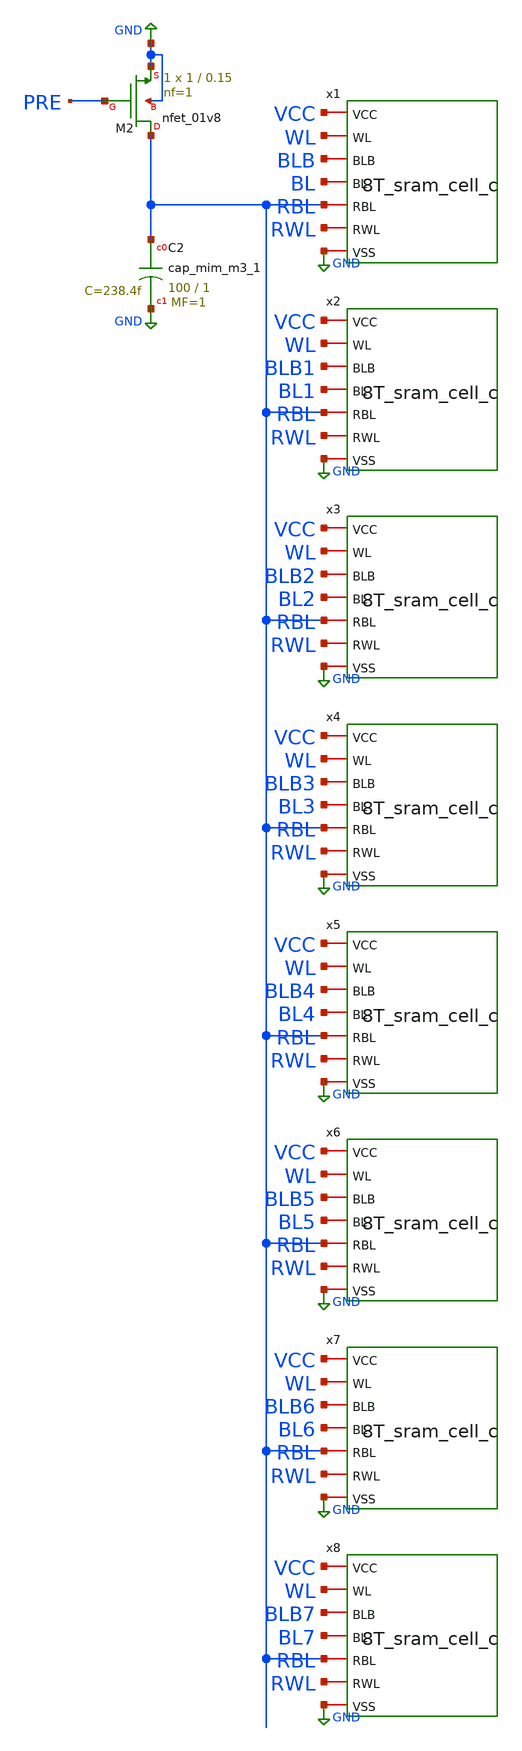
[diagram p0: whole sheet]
** sch_path: 8T_sram_c_array_mactest.sch
**.subckt 8T_sram_c_array_mactest
x1 VCC WL BLB BL RBL RWL GND 8T_sram_cell_c
XC2 RBL GND sky130_fd_pr__cap_mim_m3_1 W=100 L=1 MF=1 m=1
x2 VCC WL BLB1 BL1 RBL RWL GND 8T_sram_cell_c
x3 VCC WL BLB2 BL2 RBL RWL GND 8T_sram_cell_c
x4 VCC WL BLB3 BL3 RBL RWL GND 8T_sram_cell_c
x5 VCC WL BLB4 BL4 RBL RWL GND 8T_sram_cell_c
x6 VCC WL BLB5 BL5 RBL RWL GND 8T_sram_cell_c
x7 VCC WL BLB6 BL6 RBL RWL GND 8T_sram_cell_c
x8 VCC WL BLB7 BL7 RBL RWL GND 8T_sram_cell_c
XM2 RBL PRE GND GND sky130_fd_pr__nfet_01v8 L=0.15 W=1 nf=1 ad='int((1 + 1)/2) * 1 / 1 * 0.29' as='int((1 + 2)/2) * 1 / 1 * 0.29'
+ pd='2*int((1 + 1)/2) * (1 / 1 + 0.29)' ps='2*int((1 + 2)/2) * (1 / 1 + 0.29)' nrd='0.29 / 1 ' nrs='0.29 / 1 '
+ sa=0 sb=0 sd=0 mult=1 m=1
**** begin user architecture code


.param dly=0ns t_dly=2ns raise=10ps fall=10ps BL_period=20ns prds=128 pre_time=2ns read_time=0.5ns

**vss vss 0 DC 0
* PULSE(VSS 1.8 2ns 100ps 100ps 3ns 5ns 4)PULSE(0 1.7 {dly + t_dly/2} {raise} {fall} {(BL_period/2)- t_dly}
*+ {BL_period/2} {prds*2})

V_WL WL 0 PULSE({VSS} {VCC} {dly + t_dly/2} {raise} {fall} {(BL_period/2)- t_dly} {BL_period} {prds*2})


V_BL BLB 0 PULSE({VSS} {VCC} {dly} {raise} {fall} {BL_period} {BL_period*2} {prds})
V_BLB BL 0 PULSE({VCC} {VSS} {dly} {raise} {fall} {BL_period} {BL_period*2} {prds})

V_BL1 BLB1 0 PULSE({VSS} {VCC} {dly} {raise} {fall} {BL_period*2} {BL_period*4} {prds})
V_BLB1 BL1 0 PULSE({VCC} {VSS} {dly} {raise} {fall} {BL_period*2} {BL_period*4} {prds})

V_BL2 BLB2 0 PULSE({VSS} {VCC} {dly} {raise} {fall} {BL_period*4} {BL_period*8} {prds})
V_BLB2 BL2 0 PULSE({VCC} {VSS} {dly} {raise} {fall} {BL_period*4} {BL_period*8} {prds})

V_BL3 BLB3 0 PULSE({VSS} {VCC} {dly} {raise} {fall} {BL_period*8} {BL_period*16} {prds})
V_BLB3 BL3 0 PULSE({VCC} {VSS} {dly} {raise} {fall} {BL_period*8} {BL_period*16} {prds})

V_BL4 BLB4 0 PULSE({VSS} {VCC} {dly} {raise} {fall} {BL_period*16} {BL_period*32} {prds})
V_BLB4 BL4 0 PULSE({VCC} {VSS} {dly} {raise} {fall} {BL_period*16} {BL_period*32} {prds})

V_BL5 BLB5 0 PULSE({VSS} {VCC} {dly} {raise} {fall} {BL_period*32} {BL_period*64} {prds})
V_BLB5 BL5 0 PULSE({VCC} {VSS} {dly} {raise} {fall} {BL_period*32} {BL_period*64} {prds})

V_BL6 BLB6 0 PULSE({VSS} {VCC} {dly} {raise} {fall} {BL_period*64} {BL_period*128} {prds})
V_BLB6 BL6 0 PULSE({VCC} {VSS} {dly} {raise} {fall} {BL_period*64} {BL_period*128} {prds})

V_BL7 BLB7 0 PULSE({VSS} {VCC} {dly} {raise} {fall} {BL_period*128} {BL_period*256} {prds})
V_BLB7 BL7 0 PULSE({VCC} {VSS} {dly} {raise} {fall} {BL_period*128} {BL_period*256} {prds})


V_RWL RWL 0 PULSE({VCC} {VSS} {dly + BL_period/2 + 6ns} {raise} {fall} {read_time} {BL_period} {prds*2})
V_PRE PRE 0 PULSE({VSS} {VCC} {dly + BL_period/2} {raise} {fall} {pre_time} {BL_period} {prds*2})

.tran 0.01ns 5130ns uic
.control
run
* plot WL BL-2 BLB-4 RWL-6 RBL-8 PRE-10
plot RBL PRE+2 RWL+4 BL3+6 BL2+8 BL1+10 BL+12 WL+14
.endc
.save V(WL) V(BL) V(BL1) V(BL2) V(BL3) V(BL4) V(BL5) V(BL6) V(BL7) V(RWL) V(RBL) V(PRE)




** opencircuitdesign pdks install
.lib $::SKYWATER_MODELS/sky130.lib.spice tt



.param VCC=1.8 VSS=0

V_VCC VCC 0 DC 1.8
V_VSS VSS 0 DC 0


**** end user architecture code
**.ends
.GLOBAL GND
.end
